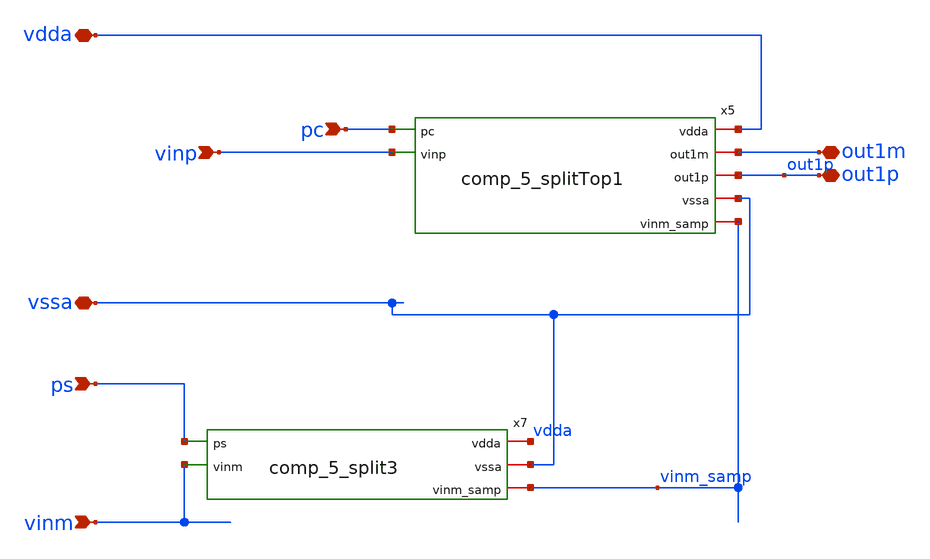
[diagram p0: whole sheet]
** sch_path: 5_Design/4_Layout/Team 5/xschem/comp_5_splitTop3.sch
**.subckt comp_5_splitTop3 pc vdda vssa vinp ps vinm out1p out1m
*.ipin pc
*.iopin vdda
*.iopin vssa
*.ipin vinp
*.ipin ps
*.ipin vinm
*.iopin out1p
*.iopin out1m
x5 vdda pc vinp out1m out1p vssa vinm_samp comp_5_splitTop1
x7 vdda vssa ps vinm_samp vinm comp_5_split3
**.ends
.end
